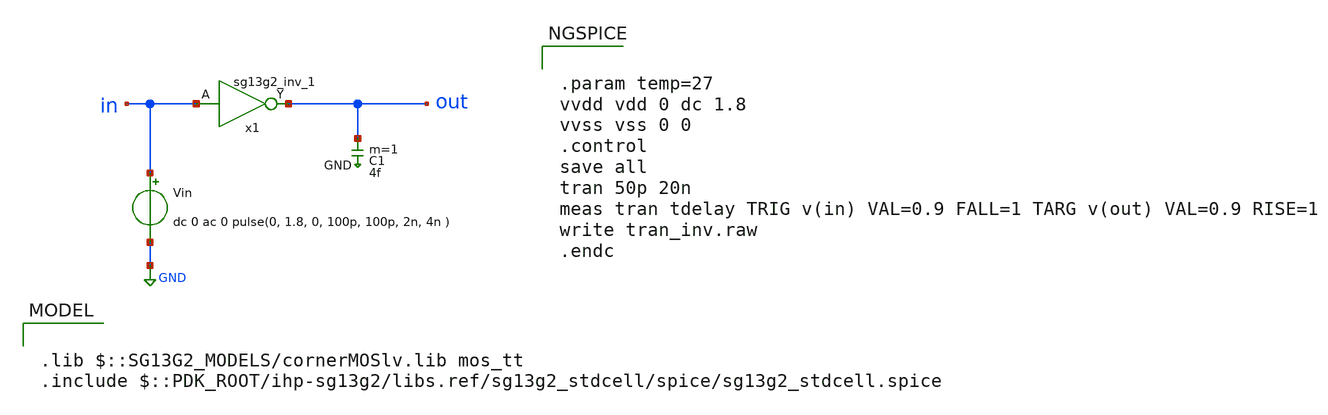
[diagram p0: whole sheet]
** sch_path: ihp-sg13g2/xschem_libs/sg13g2_stdcells/tran_inv/schematic/tran_inv.sch
* Copyright 2024 IHP PDK Authors

.lib $::SG13G2_MODELS/cornerMOSlv.lib mos_tt
.include $::PDK_ROOT/ihp-sg13g2/libs.ref/sg13g2_stdcell/spice/sg13g2_stdcell.spice

**.subckt tran_inv
Vin in GND dc 0 ac 0 pulse(0, 1.8, 0, 100p, 100p, 2n, 4n )
x1 out in VDD VSS sg13g2_inv_1
C1 out GND 4f m=1
**** begin user architecture code


.param temp=27
vvdd vdd 0 dc 1.8
vvss vss 0 0
.control
save all
tran 50p 20n
meas tran tdelay TRIG v(in) VAL=0.9 FALL=1 TARG v(out) VAL=0.9 RISE=1
write tran_inv.raw
.endc


**** end user architecture code
**.ends

* expanding   symbol:  sg13g2_stdcells/sg13g2_inv_1.sym # of pins=2
** sym_path: sg13g2_stdcells/sg13g2_inv_1.sym
** sch_path: sg13g2_stdcells/sg13g2_inv_1.sch
.subckt sg13g2_inv_1 Y A VDD VSS
*.opin Y
*.ipin A
*.iopin VDD
*.iopin VSS
XM1 Y A VSS VSS sg13_lv_nmos w=740.00n l=130.00n ng=1 m=1
XM2 Y A VDD VDD sg13_lv_pmos w=1.12u l=130.00n ng=1 m=1
.ends

.GLOBAL GND
.end
